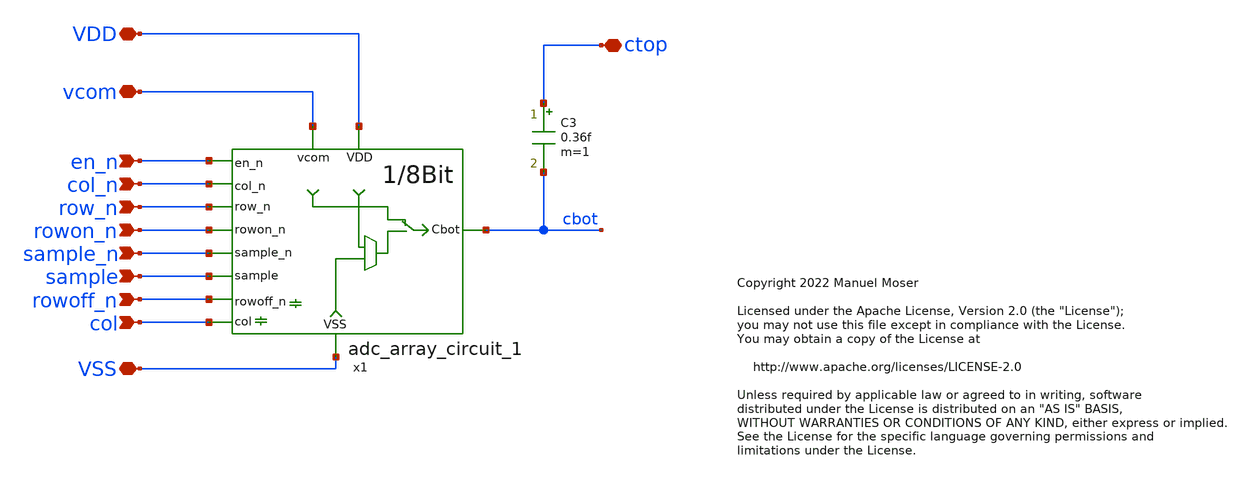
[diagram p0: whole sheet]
** sch_path: xschem/adc_array_wafflecap_8_1.sch
* Copyright 2022 Manuel Moser
* Licensed under the Apache License, Version 2.0 (the "License");
**.subckt adc_array_wafflecap_8_1 vcom VDD ctop VSS en_n row_n col_n rowon_n sample_n sample
*+ rowoff_n col
*.iopin vcom
*.iopin VDD
*.iopin ctop
*.iopin VSS
*.ipin en_n
*.ipin row_n
*.ipin col_n
*.ipin rowon_n
*.ipin sample_n
*.ipin sample
*.ipin rowoff_n
*.ipin col
C3 ctop cbot 0.36f m=1
x1 VDD col_n cbot row_n rowon_n sample_n vcom sample VSS en_n rowoff_n col adc_array_circuit_1
**.ends

* expanding   symbol:  adc_array_circuit_1.sym # of pins=12
** sym_path: xschem/adc_array_circuit_1.sym
** sch_path: xschem/adc_array_circuit_1.sch
.subckt adc_array_circuit_1 VDD col_n Cbot row_n rowon_n sample_n vcom sample VSS en_n rowoff_n col
*.ipin sample_n
*.ipin sample
*.iopin vcom
*.ipin row_n
*.ipin col_n
*.ipin rowon_n
*.iopin VDD
*.iopin VSS
*.iopin Cbot
*.ipin en_n
*.ipin rowoff_n
*.ipin col
XM1 vcom sample Cbot VSS sky130_fd_pr__nfet_01v8 L=0.15 W=0.42 nf=1 ad='int((nf+1)/2) * W/nf * 0.29'
+ as='int((nf+2)/2) * W/nf * 0.29' pd='2*int((nf+1)/2) * (W/nf + 0.29)' ps='2*int((nf+2)/2) * (W/nf + 0.29)'
+ nrd='0.29 / W' nrs='0.29 / W' sa=0 sb=0 sd=0 mult=1 m=1
XM3 vcom sample_n Cbot VDD sky130_fd_pr__pfet_01v8 L=0.15 W=0.8 nf=1 ad='int((nf+1)/2) * W/nf * 0.29'
+ as='int((nf+2)/2) * W/nf * 0.29' pd='2*int((nf+1)/2) * (W/nf + 0.29)' ps='2*int((nf+2)/2) * (W/nf + 0.29)'
+ nrd='0.29 / W' nrs='0.29 / W' sa=0 sb=0 sd=0 mult=1 m=1
XM2 vdrv sample_n Cbot VSS sky130_fd_pr__nfet_01v8 L=0.15 W=0.42 nf=1 ad='int((nf+1)/2) * W/nf * 0.29'
+ as='int((nf+2)/2) * W/nf * 0.29' pd='2*int((nf+1)/2) * (W/nf + 0.29)' ps='2*int((nf+2)/2) * (W/nf + 0.29)'
+ nrd='0.29 / W' nrs='0.29 / W' sa=0 sb=0 sd=0 mult=1 m=1
XM4 vdrv sample Cbot VDD sky130_fd_pr__pfet_01v8 L=0.15 W=0.8 nf=1 ad='int((nf+1)/2) * W/nf * 0.29' as='int((nf+2)/2) * W/nf * 0.29'
+ pd='2*int((nf+1)/2) * (W/nf + 0.29)' ps='2*int((nf+2)/2) * (W/nf + 0.29)' nrd='0.29 / W' nrs='0.29 / W'
+ sa=0 sb=0 sd=0 mult=1 m=1
XM5 vint1 en_n vdrv VDD sky130_fd_pr__pfet_01v8 L=0.15 W=0.8 nf=1 ad='int((nf+1)/2) * W/nf * 0.29' as='int((nf+2)/2) * W/nf * 0.29'
+ pd='2*int((nf+1)/2) * (W/nf + 0.29)' ps='2*int((nf+2)/2) * (W/nf + 0.29)' nrd='0.29 / W' nrs='0.29 / W'
+ sa=0 sb=0 sd=0 mult=1 m=1
XM6 VDD en_n vint1 VDD sky130_fd_pr__pfet_01v8 L=0.15 W=0.8 nf=1 ad='int((nf+1)/2) * W/nf * 0.29' as='int((nf+2)/2) * W/nf * 0.29'
+ pd='2*int((nf+1)/2) * (W/nf + 0.29)' ps='2*int((nf+2)/2) * (W/nf + 0.29)' nrd='0.29 / W' nrs='0.29 / W'
+ sa=0 sb=0 sd=0 mult=1 m=1
XM7 VDD en_n vdrv VDD sky130_fd_pr__pfet_01v8 L=0.15 W=0.8 nf=1 ad='int((nf+1)/2) * W/nf * 0.29' as='int((nf+2)/2) * W/nf * 0.29'
+ pd='2*int((nf+1)/2) * (W/nf + 0.29)' ps='2*int((nf+2)/2) * (W/nf + 0.29)' nrd='0.29 / W' nrs='0.29 / W'
+ sa=0 sb=0 sd=0 mult=1 m=1
XM8 vint2 en_n vdrv VSS sky130_fd_pr__nfet_01v8 L=0.15 W=0.42 nf=1 ad='int((nf+1)/2) * W/nf * 0.29' as='int((nf+2)/2) * W/nf * 0.29'
+ pd='2*int((nf+1)/2) * (W/nf + 0.29)' ps='2*int((nf+2)/2) * (W/nf + 0.29)' nrd='0.29 / W' nrs='0.29 / W'
+ sa=0 sb=0 sd=0 mult=1 m=1
XM9 VSS en_n vint2 VSS sky130_fd_pr__nfet_01v8 L=0.15 W=0.42 nf=1 ad='int((nf+1)/2) * W/nf * 0.29' as='int((nf+2)/2) * W/nf * 0.29'
+ pd='2*int((nf+1)/2) * (W/nf + 0.29)' ps='2*int((nf+2)/2) * (W/nf + 0.29)' nrd='0.29 / W' nrs='0.29 / W'
+ sa=0 sb=0 sd=0 mult=1 m=1
XM10 VSS en_n vint2 VSS sky130_fd_pr__nfet_01v8 L=0.15 W=0.42 nf=1 ad='int((nf+1)/2) * W/nf * 0.29' as='int((nf+2)/2) * W/nf * 0.29'
+ pd='2*int((nf+1)/2) * (W/nf + 0.29)' ps='2*int((nf+2)/2) * (W/nf + 0.29)' nrd='0.29 / W' nrs='0.29 / W'
+ sa=0 sb=0 sd=0 mult=1 m=1
* noconn row_n
* noconn col_n
* noconn rowon_n
* noconn rowoff_n
* noconn col
.ends

.end
